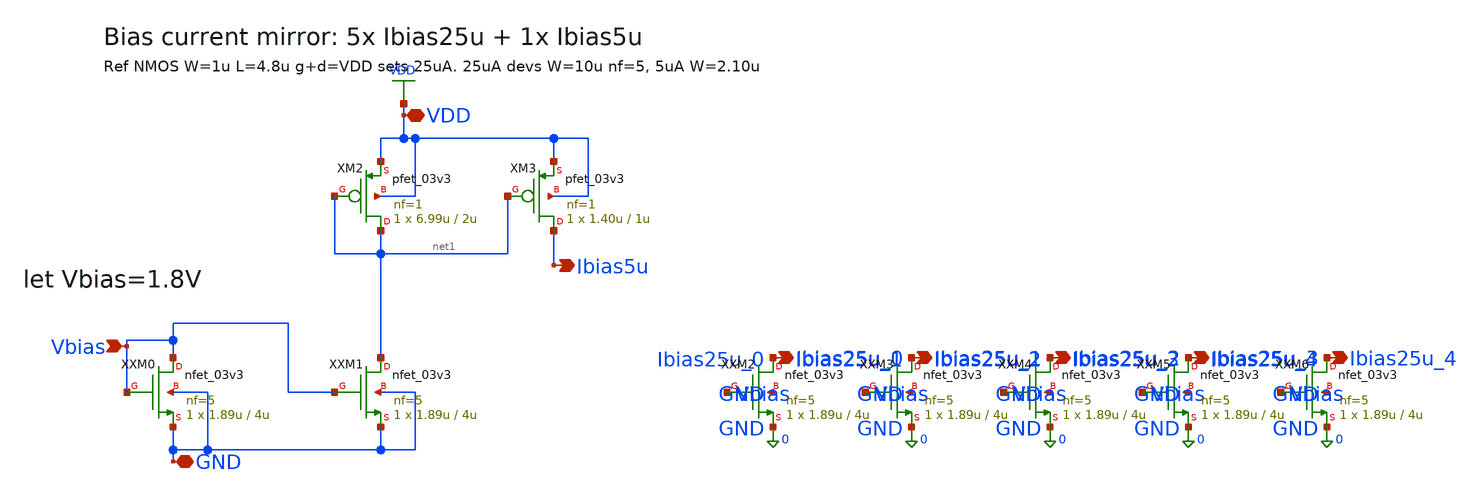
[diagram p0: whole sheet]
** sch_path: ps-bias/jz_bias.sch
**.subckt jz_bias Ibias25u_0 Ibias25u_1 Ibias25u_2 Ibias25u_3 Ibias25u_4 Ibias5u VDD GND Vbias
*.opin Ibias25u_0
*.opin Ibias25u_1
*.opin Ibias25u_2
*.opin Ibias25u_3
*.opin Ibias25u_4
*.opin Ibias5u
*.iopin VDD
*.iopin GND
*.ipin Vbias
XXM0 Vbias Vbias GND GND nfet_03v3 L=4u W=1.89u nf=5 ad='int((nf+1)/2) * W/nf * 0.18u' as='int((nf+2)/2) * W/nf * 0.18u'
+ pd='2*int((nf+1)/2) * (W/nf + 0.18u)' ps='2*int((nf+2)/2) * (W/nf + 0.18u)' nrd='0.18u / W' nrs='0.18u / W'
+ sa=0 sb=0 sd=0 m=1
XM2 net1 net1 VDD VDD pfet_03v3 L=2u W=6.99u nf=1 ad='int((nf+1)/2) * W/nf * 0.18u' as='int((nf+2)/2) * W/nf * 0.18u'
+ pd='2*int((nf+1)/2) * (W/nf + 0.18u)' ps='2*int((nf+2)/2) * (W/nf + 0.18u)' nrd='0.18u / W' nrs='0.18u / W'
+ sa=0 sb=0 sd=0 m=1
XM3 Ibias5u net1 VDD VDD pfet_03v3 L=1u W=1.40u nf=1 ad='int((nf+1)/2) * W/nf * 0.18u' as='int((nf+2)/2) * W/nf * 0.18u'
+ pd='2*int((nf+1)/2) * (W/nf + 0.18u)' ps='2*int((nf+2)/2) * (W/nf + 0.18u)' nrd='0.18u / W' nrs='0.18u / W'
+ sa=0 sb=0 sd=0 m=1
XXM1 net1 Vbias GND GND nfet_03v3 L=4u W=1.89u nf=5 ad='int((nf+1)/2) * W/nf * 0.18u' as='int((nf+2)/2) * W/nf * 0.18u'
+ pd='2*int((nf+1)/2) * (W/nf + 0.18u)' ps='2*int((nf+2)/2) * (W/nf + 0.18u)' nrd='0.18u / W' nrs='0.18u / W'
+ sa=0 sb=0 sd=0 m=1
XXM2 Ibias25u_0 Vbias GND GND nfet_03v3 L=4u W=1.89u nf=5 ad='int((nf+1)/2) * W/nf * 0.18u' as='int((nf+2)/2) * W/nf * 0.18u'
+ pd='2*int((nf+1)/2) * (W/nf + 0.18u)' ps='2*int((nf+2)/2) * (W/nf + 0.18u)' nrd='0.18u / W' nrs='0.18u / W'
+ sa=0 sb=0 sd=0 m=1
XXM3 Ibias25u_1 Vbias GND GND nfet_03v3 L=4u W=1.89u nf=5 ad='int((nf+1)/2) * W/nf * 0.18u' as='int((nf+2)/2) * W/nf * 0.18u'
+ pd='2*int((nf+1)/2) * (W/nf + 0.18u)' ps='2*int((nf+2)/2) * (W/nf + 0.18u)' nrd='0.18u / W' nrs='0.18u / W'
+ sa=0 sb=0 sd=0 m=1
XXM4 Ibias25u_2 Vbias GND GND nfet_03v3 L=4u W=1.89u nf=5 ad='int((nf+1)/2) * W/nf * 0.18u' as='int((nf+2)/2) * W/nf * 0.18u'
+ pd='2*int((nf+1)/2) * (W/nf + 0.18u)' ps='2*int((nf+2)/2) * (W/nf + 0.18u)' nrd='0.18u / W' nrs='0.18u / W'
+ sa=0 sb=0 sd=0 m=1
XXM5 Ibias25u_3 Vbias GND GND nfet_03v3 L=4u W=1.89u nf=5 ad='int((nf+1)/2) * W/nf * 0.18u' as='int((nf+2)/2) * W/nf * 0.18u'
+ pd='2*int((nf+1)/2) * (W/nf + 0.18u)' ps='2*int((nf+2)/2) * (W/nf + 0.18u)' nrd='0.18u / W' nrs='0.18u / W'
+ sa=0 sb=0 sd=0 m=1
XXM6 Ibias25u_4 Vbias GND GND nfet_03v3 L=4u W=1.89u nf=5 ad='int((nf+1)/2) * W/nf * 0.18u' as='int((nf+2)/2) * W/nf * 0.18u'
+ pd='2*int((nf+1)/2) * (W/nf + 0.18u)' ps='2*int((nf+2)/2) * (W/nf + 0.18u)' nrd='0.18u / W' nrs='0.18u / W'
+ sa=0 sb=0 sd=0 m=1
**.ends
.GLOBAL VDD
.end
